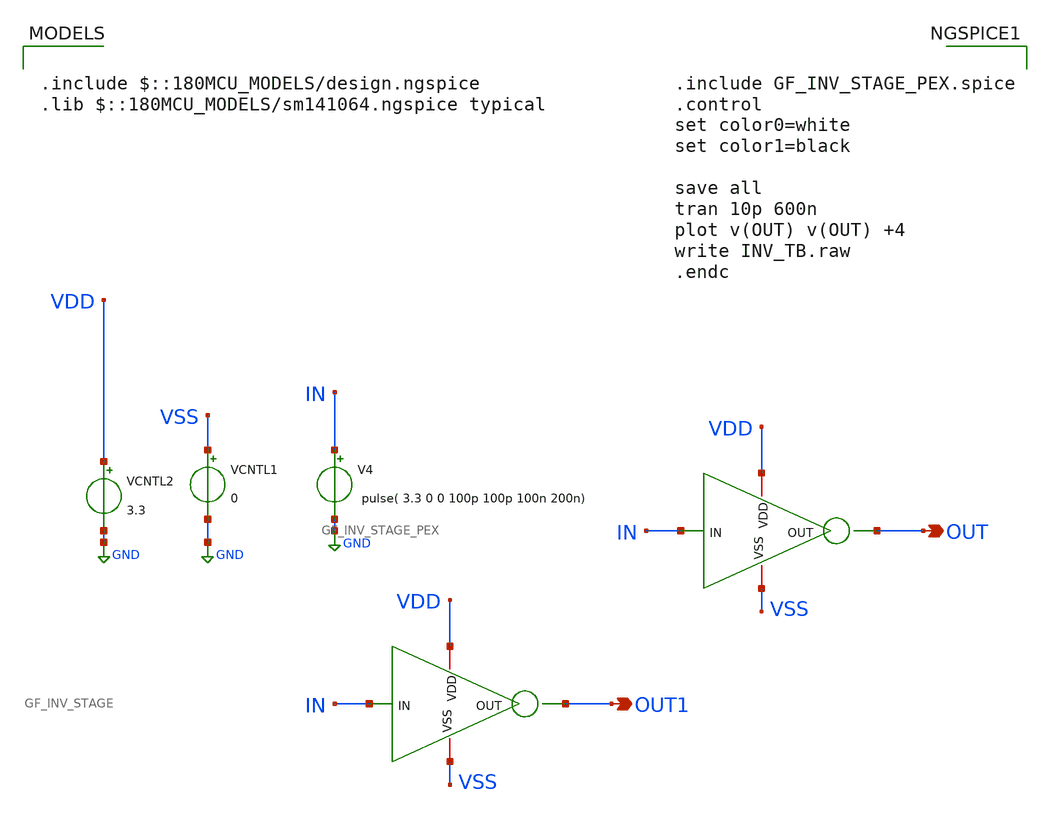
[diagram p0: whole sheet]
** sch_path: Clock_Generator_PAKISTAN_02/xschem/INV_TB.sch
**.subckt INV_TB OUT OUT1
*.opin OUT
*.opin OUT1
V4 IN GND pulse( 3.3 0 0 100p 100p 100n 200n)
VCNTL1 VSS GND 0
VCNTL2 VDD GND 3.3
x1 VSS VDD OUT1 IN GF_INV_STAGE
x2 VSS VDD OUT IN GF_INV_STAGE_PEX
**** begin user architecture code


.include GF_INV_STAGE_PEX.spice
.control
set color0=white
set color1=black

save all
tran 10p 600n
plot v(OUT) v(OUT) +4
write INV_TB.raw
.endc



.include $::180MCU_MODELS/design.ngspice
.lib $::180MCU_MODELS/sm141064.ngspice typical

**** end user architecture code
**.ends
.GLOBAL GND
.end
